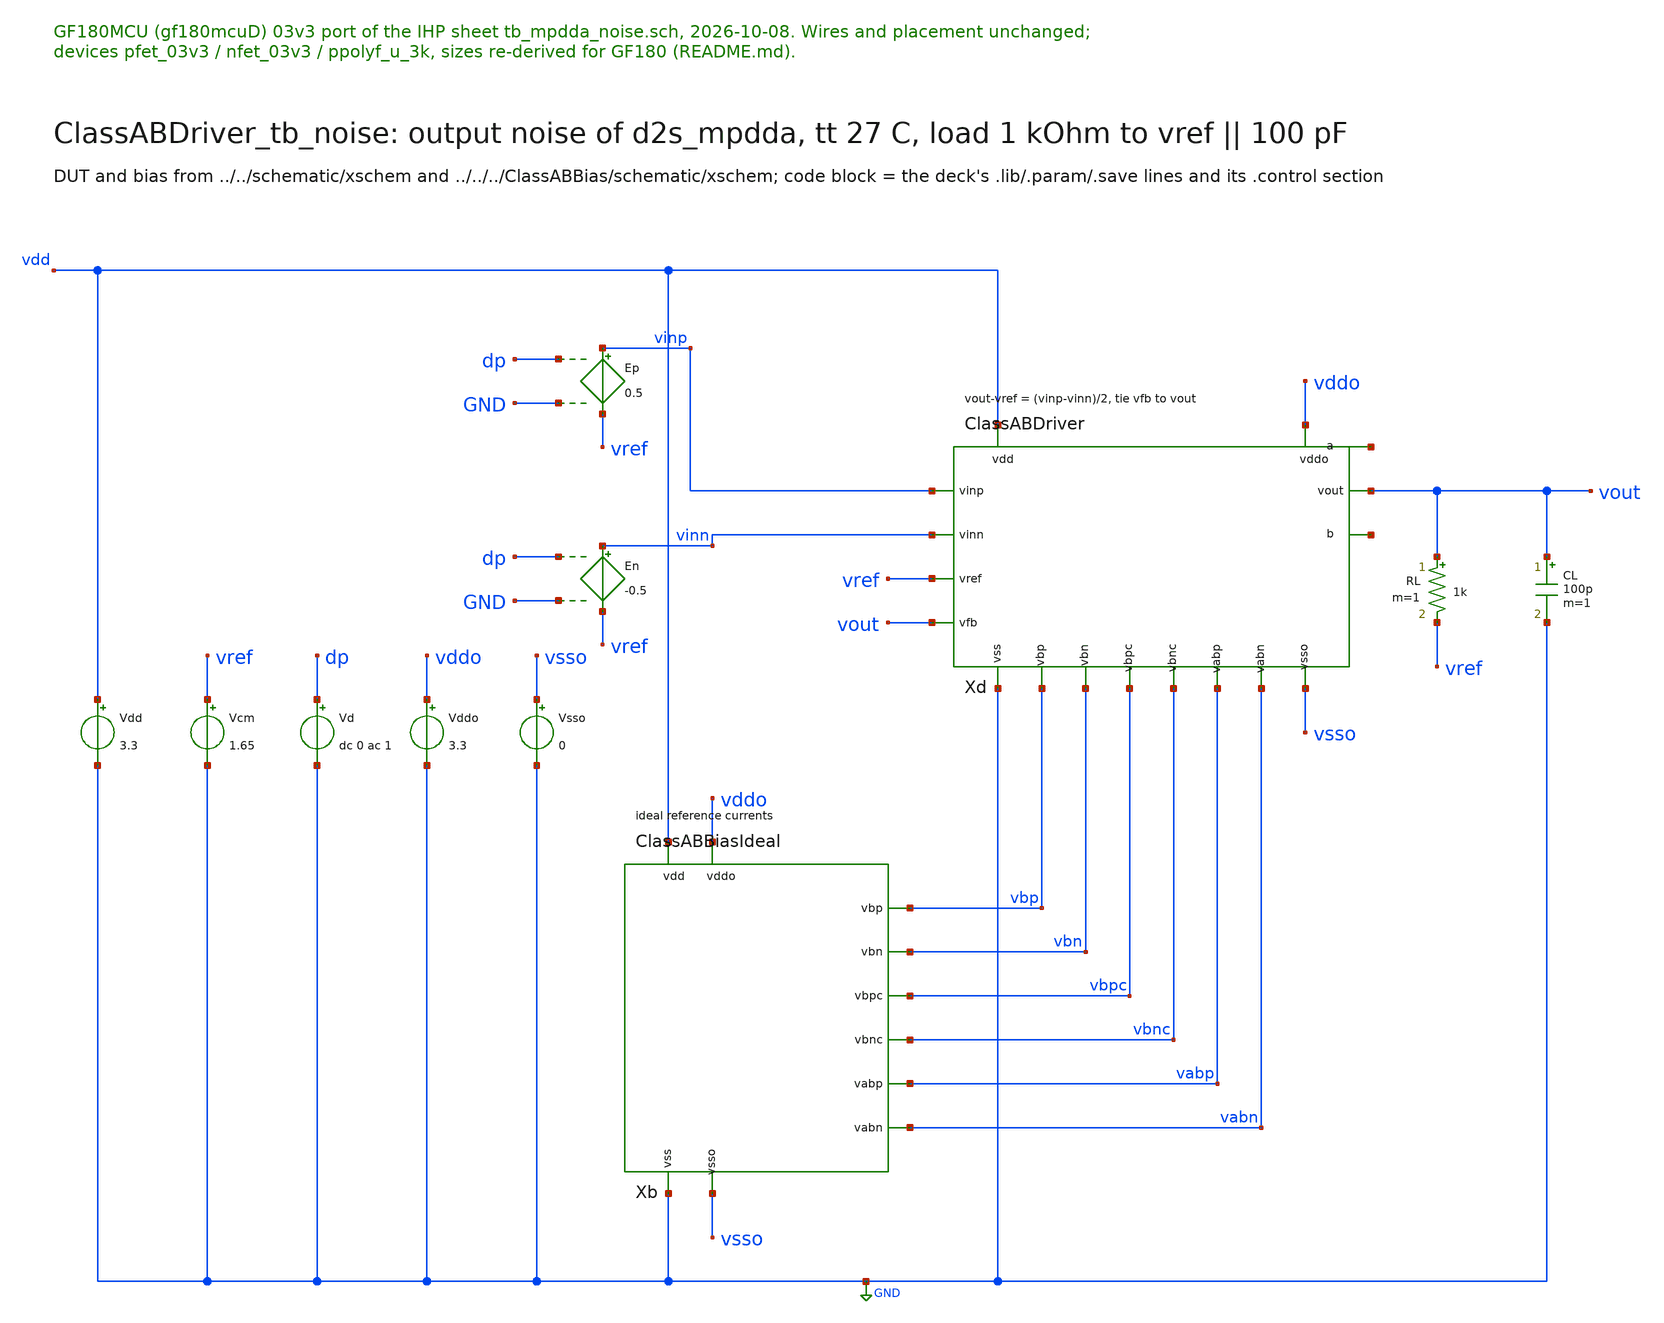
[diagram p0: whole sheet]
** sch_path: macros/ClassABDriver/testbenches/xschem/ClassABDriver_tb_noise.sch
**.subckt ClassABDriver_tb_noise
Vdd vdd GND 3.3
Vcm vref GND 1.65
Xb vdd GND vddo vsso vbp vbn vbpc vbnc vabp vabn ClassABBiasIdeal
Xd vdd GND vddo vsso vinp vinn vref vout vout vbp vbn vbpc vbnc vabp vabn net1 net2 ClassABDriver
Vd dp GND dc 0 ac 1
Ep vinp vref dp GND 0.5
En vinn vref dp GND -0.5
RL vout vref 1k m=1
CL vout GND 100p m=1
Vddo vddo GND 3.3
Vsso vsso GND 0
**** begin user architecture code

.control
* integrated noise first (plots noise1 = spectrum, noise2 = total), then two spot values
noise v(vout) Vd dec 20 10 10meg
setplot noise2
print onoise_total
noise v(vout) Vd lin 1 1k 1k
noise v(vout) Vd lin 1 100k 100k
* a one-point noise run makes only a spectrum plot: noise3 (1 kHz), noise4 (100 kHz)
print noise3.onoise_spectrum noise4.onoise_spectrum
if $?batchmode = 0
  setplot noise1
  plot onoise_spectrum loglog
end
.endc


.include $::180MCU_MODELS/design.ngspice
.lib $::180MCU_MODELS/sm141064.ngspice typical
.lib $::180MCU_MODELS/sm141064.ngspice res_typical
.lib $::180MCU_MODELS/sm141064.ngspice moscap_typical

**** end user architecture code
**.ends
.GLOBAL GND
.end
